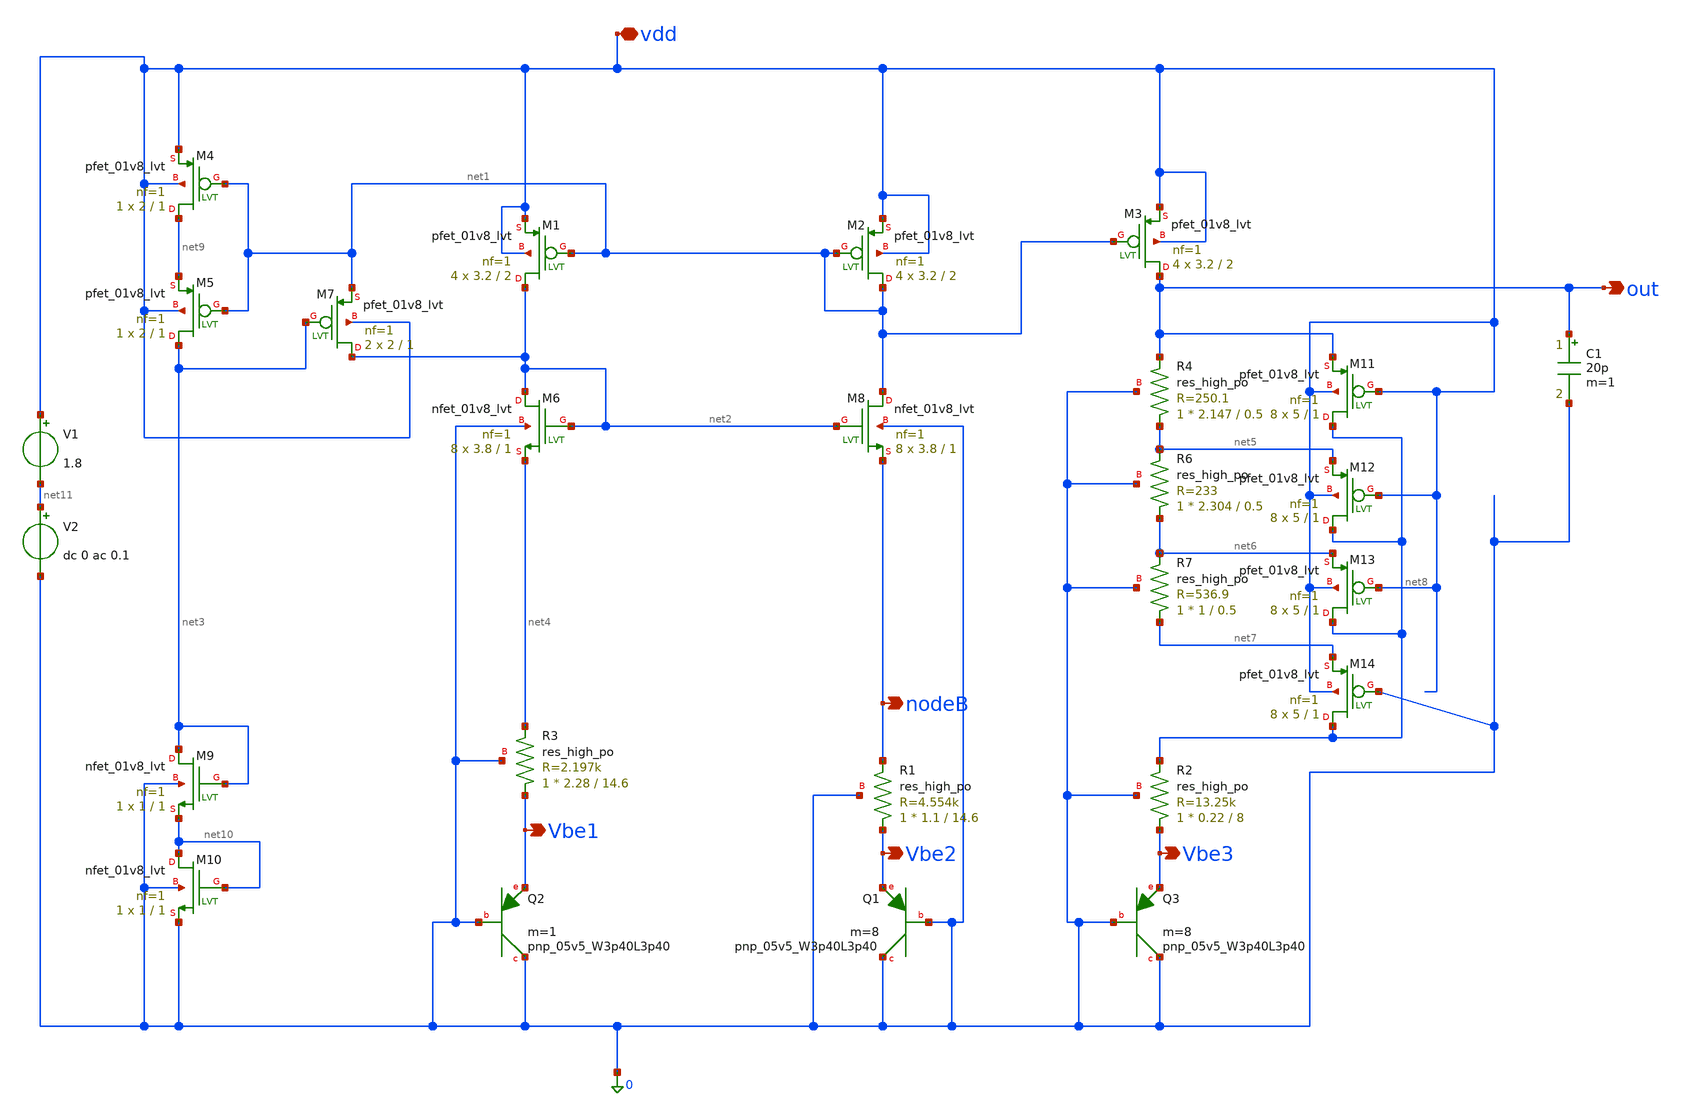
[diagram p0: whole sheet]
** sch_path: BGR_TOP_SKY130A/TB_BGR_v2.sch
**.subckt TB_BGR_v2 vdd out nodeB Vbe1 Vbe2 Vbe3
*.iopin vdd
*.opin out
*.opin nodeB
*.opin Vbe1
*.opin Vbe2
*.opin Vbe3
XM6 net2 net2 net4 0 sky130_fd_pr__nfet_01v8_lvt L=1 W=3.8 nf=1 ad='int((1 + 1)/2) * 3.8 / 1 * 0.29'
+ as='int((1 + 2)/2) * 3.8 / 1 * 0.29' pd='2*int((1 + 1)/2) * (3.8 / 1 + 0.29)' ps='2*int((1 + 2)/2) * (3.8 / 1 + 0.29)'
+ nrd='0.29 / 3.8 ' nrs='0.29 / 3.8 ' sa=0 sb=0 sd=0 mult=8 m=8
XM1 net2 net1 vdd vdd sky130_fd_pr__pfet_01v8_lvt L=2 W=3.2 nf=1 ad='int((1 + 1)/2) * 3.2 / 1 * 0.29'
+ as='int((1 + 2)/2) * 3.2 / 1 * 0.29' pd='2*int((1 + 1)/2) * (3.2 / 1 + 0.29)' ps='2*int((1 + 2)/2) * (3.2 / 1 + 0.29)'
+ nrd='0.29 / 3.2 ' nrs='0.29 / 3.2 ' sa=0 sb=0 sd=0 mult=4 m=4
XQ1 0 0 Vbe2 sky130_fd_pr__pnp_05v5_W3p40L3p40 m=8
XR1 Vbe2 nodeB 0 sky130_fd_pr__res_high_po W=1.1 L=14.6 mult=1 m=1
XM3 out net1 vdd vdd sky130_fd_pr__pfet_01v8_lvt L=2 W=3.2 nf=1 ad='int((1 + 1)/2) * 3.2 / 1 * 0.29'
+ as='int((1 + 2)/2) * 3.2 / 1 * 0.29' pd='2*int((1 + 1)/2) * (3.2 / 1 + 0.29)' ps='2*int((1 + 2)/2) * (3.2 / 1 + 0.29)'
+ nrd='0.29 / 3.2 ' nrs='0.29 / 3.2 ' sa=0 sb=0 sd=0 mult=4 m=4
XM4 net9 net1 vdd vdd sky130_fd_pr__pfet_01v8_lvt L=1 W=2 nf=1 ad='int((1 + 1)/2) * 2 / 1 * 0.29' as='int((1 + 2)/2) * 2 / 1 * 0.29'
+ pd='2*int((1 + 1)/2) * (2 / 1 + 0.29)' ps='2*int((1 + 2)/2) * (2 / 1 + 0.29)' nrd='0.29 / 2 ' nrs='0.29 / 2 '
+ sa=0 sb=0 sd=0 mult=1 m=1
XM2 net1 net1 vdd vdd sky130_fd_pr__pfet_01v8_lvt L=2 W=3.2 nf=1 ad='int((1 + 1)/2) * 3.2 / 1 * 0.29'
+ as='int((1 + 2)/2) * 3.2 / 1 * 0.29' pd='2*int((1 + 1)/2) * (3.2 / 1 + 0.29)' ps='2*int((1 + 2)/2) * (3.2 / 1 + 0.29)'
+ nrd='0.29 / 3.2 ' nrs='0.29 / 3.2 ' sa=0 sb=0 sd=0 mult=4 m=4
XM7 net2 net3 net1 vdd sky130_fd_pr__pfet_01v8_lvt L=1 W=2 nf=1 ad='int((1 + 1)/2) * 2 / 1 * 0.29' as='int((1 + 2)/2) * 2 / 1 * 0.29'
+ pd='2*int((1 + 1)/2) * (2 / 1 + 0.29)' ps='2*int((1 + 2)/2) * (2 / 1 + 0.29)' nrd='0.29 / 2 ' nrs='0.29 / 2 '
+ sa=0 sb=0 sd=0 mult=2 m=2
XM8 net1 net2 nodeB 0 sky130_fd_pr__nfet_01v8_lvt L=1 W=3.8 nf=1 ad='int((1 + 1)/2) * 3.8 / 1 * 0.29'
+ as='int((1 + 2)/2) * 3.8 / 1 * 0.29' pd='2*int((1 + 1)/2) * (3.8 / 1 + 0.29)' ps='2*int((1 + 2)/2) * (3.8 / 1 + 0.29)'
+ nrd='0.29 / 3.8 ' nrs='0.29 / 3.8 ' sa=0 sb=0 sd=0 mult=8 m=8
XM9 net3 net3 net10 0 sky130_fd_pr__nfet_01v8_lvt L=1 W=1 nf=1 ad='int((1 + 1)/2) * 1 / 1 * 0.29' as='int((1 + 2)/2) * 1 / 1 * 0.29'
+ pd='2*int((1 + 1)/2) * (1 / 1 + 0.29)' ps='2*int((1 + 2)/2) * (1 / 1 + 0.29)' nrd='0.29 / 1 ' nrs='0.29 / 1 '
+ sa=0 sb=0 sd=0 mult=1 m=1
XQ2 0 0 Vbe1 sky130_fd_pr__pnp_05v5_W3p40L3p40 m=1
XQ3 0 0 Vbe3 sky130_fd_pr__pnp_05v5_W3p40L3p40 m=8
XR2 Vbe3 net8 0 sky130_fd_pr__res_high_po W=0.22 L=8 mult=1 m=1
V1 vdd net11 1.8
XR3 Vbe1 net4 0 sky130_fd_pr__res_high_po W=2.28 L=14.6 mult=1 m=1
XM11 net8 vdd out vdd sky130_fd_pr__pfet_01v8_lvt L=1 W=5 nf=1 ad='int((1 + 1)/2) * 5 / 1 * 0.29' as='int((1 + 2)/2) * 5 / 1 * 0.29'
+ pd='2*int((1 + 1)/2) * (5 / 1 + 0.29)' ps='2*int((1 + 2)/2) * (5 / 1 + 0.29)' nrd='0.29 / 5 ' nrs='0.29 / 5 '
+ sa=0 sb=0 sd=0 mult=8 m=8
XM12 net8 vdd net5 vdd sky130_fd_pr__pfet_01v8_lvt L=1 W=5 nf=1 ad='int((1 + 1)/2) * 5 / 1 * 0.29' as='int((1 + 2)/2) * 5 / 1 * 0.29'
+ pd='2*int((1 + 1)/2) * (5 / 1 + 0.29)' ps='2*int((1 + 2)/2) * (5 / 1 + 0.29)' nrd='0.29 / 5 ' nrs='0.29 / 5 '
+ sa=0 sb=0 sd=0 mult=8 m=8
XM13 net8 vdd net6 vdd sky130_fd_pr__pfet_01v8_lvt L=1 W=5 nf=1 ad='int((1 + 1)/2) * 5 / 1 * 0.29' as='int((1 + 2)/2) * 5 / 1 * 0.29'
+ pd='2*int((1 + 1)/2) * (5 / 1 + 0.29)' ps='2*int((1 + 2)/2) * (5 / 1 + 0.29)' nrd='0.29 / 5 ' nrs='0.29 / 5 '
+ sa=0 sb=0 sd=0 mult=8 m=8
XM14 net8 0 net7 vdd sky130_fd_pr__pfet_01v8_lvt L=1 W=5 nf=1 ad='int((1 + 1)/2) * 5 / 1 * 0.29' as='int((1 + 2)/2) * 5 / 1 * 0.29'
+ pd='2*int((1 + 1)/2) * (5 / 1 + 0.29)' ps='2*int((1 + 2)/2) * (5 / 1 + 0.29)' nrd='0.29 / 5 ' nrs='0.29 / 5 '
+ sa=0 sb=0 sd=0 mult=8 m=8
XM5 net3 net1 net9 vdd sky130_fd_pr__pfet_01v8_lvt L=1 W=2 nf=1 ad='int((1 + 1)/2) * 2 / 1 * 0.29' as='int((1 + 2)/2) * 2 / 1 * 0.29'
+ pd='2*int((1 + 1)/2) * (2 / 1 + 0.29)' ps='2*int((1 + 2)/2) * (2 / 1 + 0.29)' nrd='0.29 / 2 ' nrs='0.29 / 2 '
+ sa=0 sb=0 sd=0 mult=1 m=1
XM10 net10 net10 0 0 sky130_fd_pr__nfet_01v8_lvt L=1 W=1 nf=1 ad='int((1 + 1)/2) * 1 / 1 * 0.29' as='int((1 + 2)/2) * 1 / 1 * 0.29'
+ pd='2*int((1 + 1)/2) * (1 / 1 + 0.29)' ps='2*int((1 + 2)/2) * (1 / 1 + 0.29)' nrd='0.29 / 1 ' nrs='0.29 / 1 '
+ sa=0 sb=0 sd=0 mult=1 m=1
V2 net11 0 dc 0 ac 0.1
C1 out 0 20p m=1
XR7 net7 net6 0 sky130_fd_pr__res_high_po W=1 L=0.5 mult=1 m=1
XR6 net6 net5 0 sky130_fd_pr__res_high_po W=2.304 L=0.5 mult=1 m=1
XR4 net5 out 0 sky130_fd_pr__res_high_po W=2.147 L=0.5 mult=1 m=1
**** begin user architecture code
.lib $::SKYWATER_MODELS/sky130.lib.spice ss


//.ac dec 100 1 20G
//.dc TEMP -40 125 5
.tran 1n 1m
.save all
.save db(v(out))
.end


**** end user architecture code
**.ends
.end
